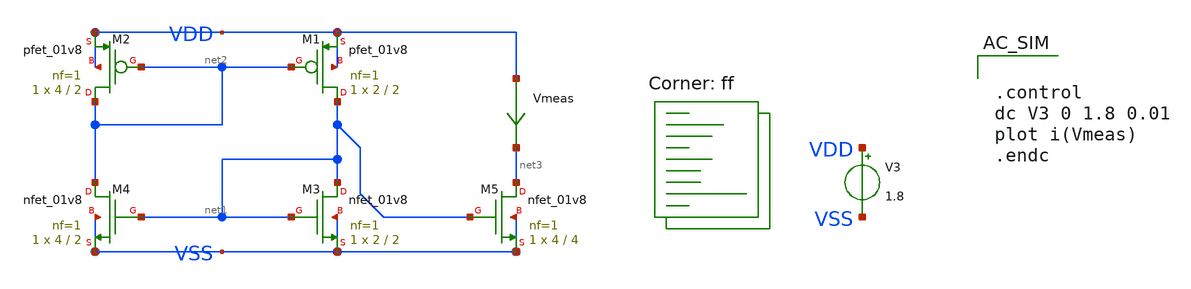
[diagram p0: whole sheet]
** sch_path: designs/libs/core_analog/core_bandgap/5t-ota/bias-net.sch
**.subckt bias-net
XM1 net1 net2 VDD VDD sky130_fd_pr__pfet_01v8 L=2 W=2 nf=1 ad='int((nf+1)/2) * W/nf * 0.29' as='int((nf+2)/2) * W/nf * 0.29'
+ pd='2*int((nf+1)/2) * (W/nf + 0.29)' ps='2*int((nf+2)/2) * (W/nf + 0.29)' nrd='0.29 / W' nrs='0.29 / W'
+ sa=0 sb=0 sd=0 mult=1 m=1
XM2 net2 net2 VDD VDD sky130_fd_pr__pfet_01v8 L=2 W=4 nf=1 ad='int((nf+1)/2) * W/nf * 0.29' as='int((nf+2)/2) * W/nf * 0.29'
+ pd='2*int((nf+1)/2) * (W/nf + 0.29)' ps='2*int((nf+2)/2) * (W/nf + 0.29)' nrd='0.29 / W' nrs='0.29 / W'
+ sa=0 sb=0 sd=0 mult=1 m=1
XM3 net1 net1 VSS VSS sky130_fd_pr__nfet_01v8 L=2 W=2 nf=1 ad='int((nf+1)/2) * W/nf * 0.29' as='int((nf+2)/2) * W/nf * 0.29'
+ pd='2*int((nf+1)/2) * (W/nf + 0.29)' ps='2*int((nf+2)/2) * (W/nf + 0.29)' nrd='0.29 / W' nrs='0.29 / W'
+ sa=0 sb=0 sd=0 mult=1 m=1
XM4 net2 net1 VSS VSS sky130_fd_pr__nfet_01v8 L=2 W=4 nf=1 ad='int((nf+1)/2) * W/nf * 0.29' as='int((nf+2)/2) * W/nf * 0.29'
+ pd='2*int((nf+1)/2) * (W/nf + 0.29)' ps='2*int((nf+2)/2) * (W/nf + 0.29)' nrd='0.29 / W' nrs='0.29 / W'
+ sa=0 sb=0 sd=0 mult=1 m=1
XM5 net3 net1 VSS VSS sky130_fd_pr__nfet_01v8 L=4 W=4 nf=1 ad='int((nf+1)/2) * W/nf * 0.29' as='int((nf+2)/2) * W/nf * 0.29'
+ pd='2*int((nf+1)/2) * (W/nf + 0.29)' ps='2*int((nf+2)/2) * (W/nf + 0.29)' nrd='0.29 / W' nrs='0.29 / W'
+ sa=0 sb=0 sd=0 mult=1 m=1
Vmeas VDD net3 0
.save i(vmeas)
V3 VDD VSS 1.8
**** begin user architecture code
.lib $::SKYWATER_MODELS/sky130.lib.spice ff


.control
dc V3 0 1.8 0.01
plot i(Vmeas)
.endc


**** end user architecture code
**.ends
.end
